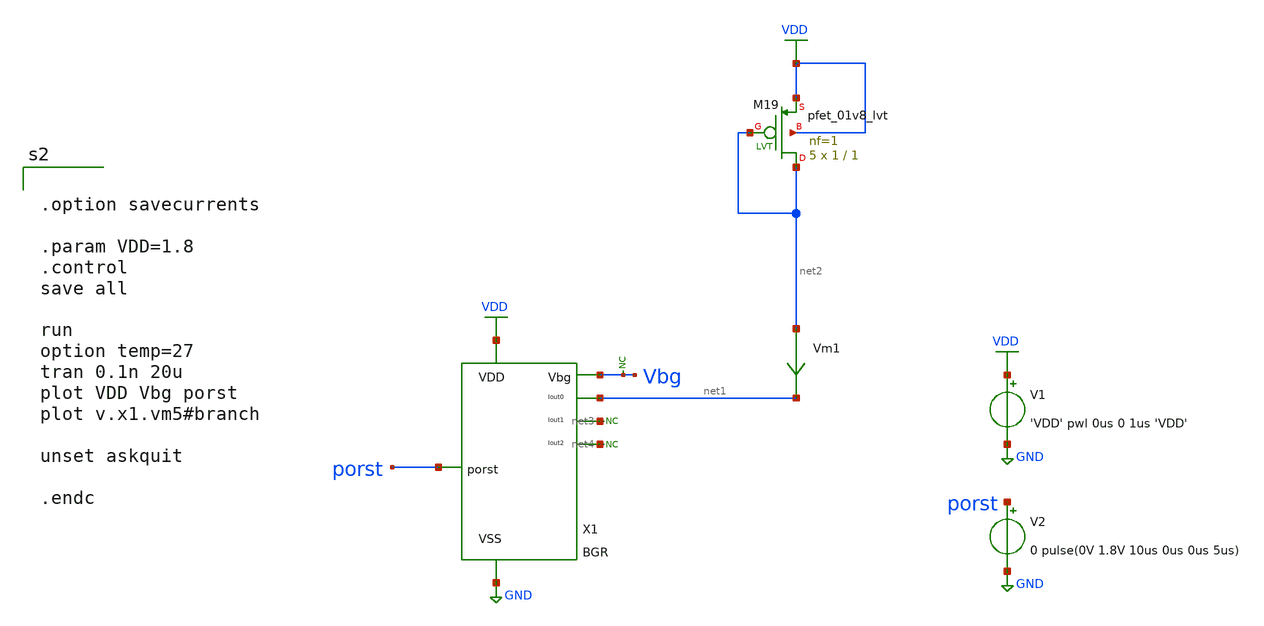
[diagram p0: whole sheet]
** sch_path: design/bgr_new/tb_BGR_tran.sch
**.subckt tb_BGR_tran
V1 VDD GND 'VDD' pwl 0us 0 1us 'VDD'
V2 porst GND 0 pulse(0V 1.8V 10us 0us 0us 5us)
* noconn #net3
* noconn #net4
XM19 net2 net2 VDD VDD sky130_fd_pr__pfet_01v8_lvt L=1 W=1 nf=1 ad='int((nf+1)/2) * W/nf * 0.29' as='int((nf+2)/2) * W/nf * 0.29'
+ pd='2*int((nf+1)/2) * (W/nf + 0.29)' ps='2*int((nf+2)/2) * (W/nf + 0.29)' nrd='0.29 / W' nrs='0.29 / W'
+ sa=0 sb=0 sd=0 mult=5 m=5
Vm1 net2 net1 0
.save i(vm1)
* noconn Vbg
X1 porst VDD GND Vbg net1 net3 net4 BGR
**** begin user architecture code

** opencircuitdesign pdks install
.lib $::SKYWATER_MODELS/sky130.lib.spice tt




.option savecurrents

.param VDD=1.8
.control
save all

run
option temp=27
tran 0.1n 20u
plot VDD Vbg porst
plot v.x1.vm5#branch

unset askquit

.endc


**** end user architecture code
**.ends
.GLOBAL VDD
.GLOBAL GND
.end
